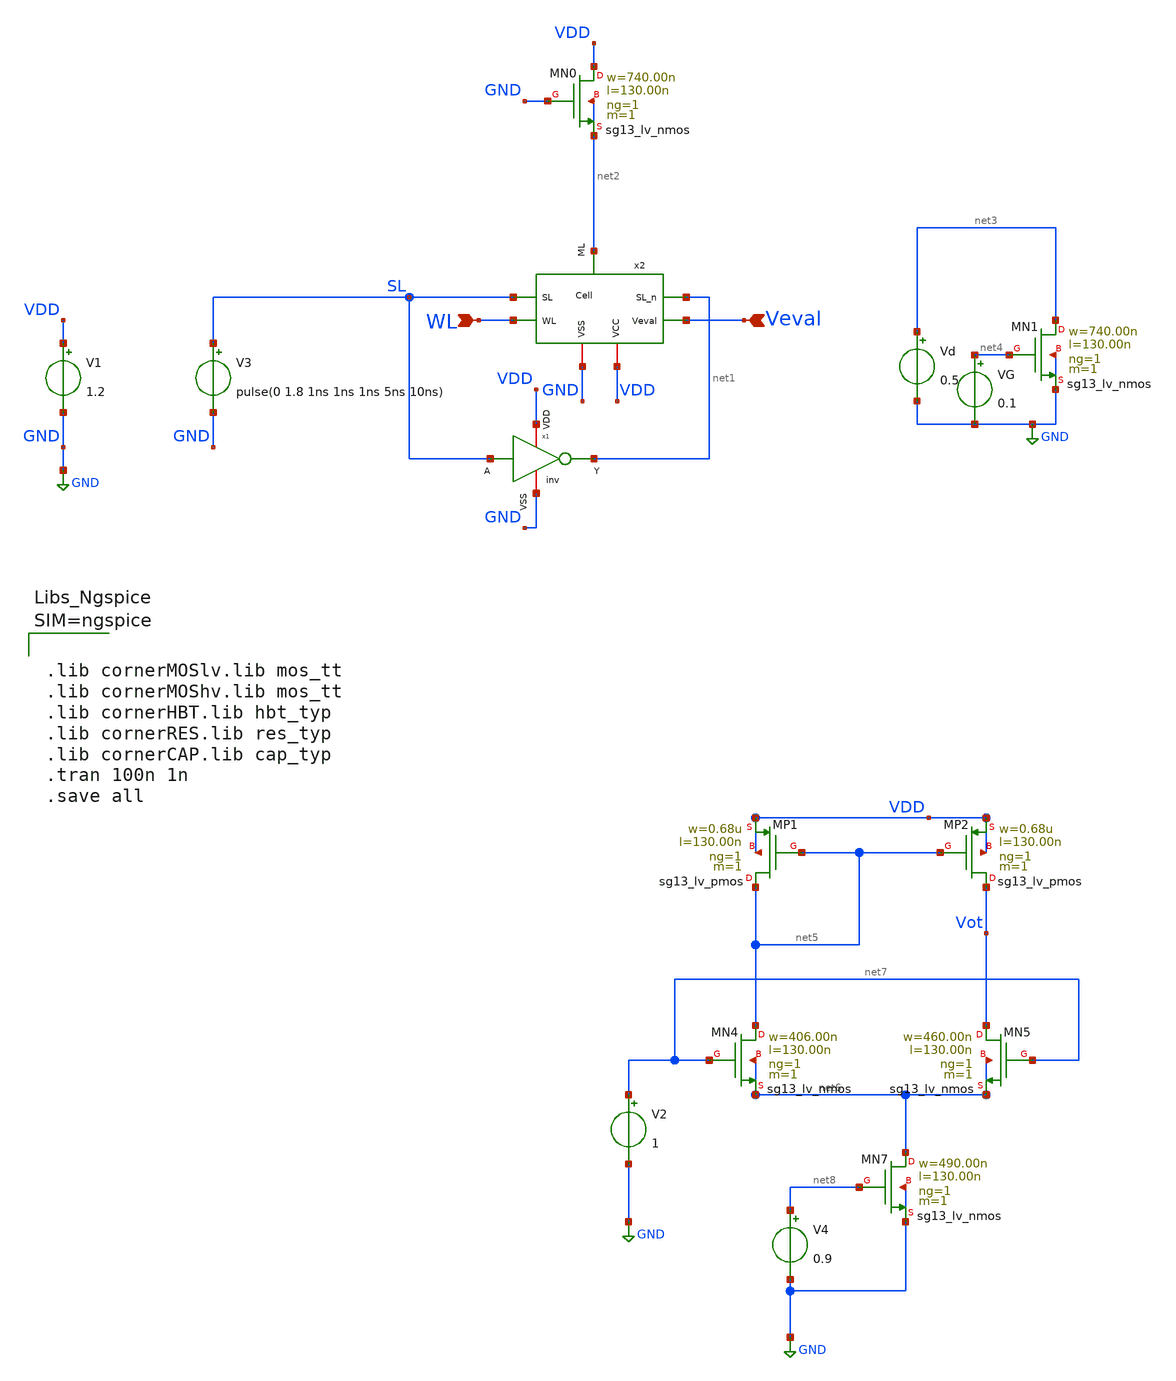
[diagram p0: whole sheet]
** sch_path: xschem/cellprobe.sch
**.subckt cellprobe WL Veval
*.ipin WL
*.ipin Veval
x2 SL WL net1 VDD net2 Veval GND Cell
V1 VDD GND 1.2
XMN0 VDD GND net2 net2 sg13_lv_nmos w=740.00n l=130.00n ng=1 m=1 mm_ok=1
V3 SL GND pulse(0 1.8 1ns 1ns 1ns 5ns 10ns)
x1 VDD net1 SL GND inv
XMN1 net3 net4 GND GND sg13_lv_nmos w=740.00n l=130.00n ng=1 m=1 mm_ok=1
Vd net3 GND 0.5
VG net4 GND 0.1
XMP1 net5 net5 VDD VDD sg13_lv_pmos w=0.68u l=130.00n ng=1 m=1 mm_ok=1
XMN4 net5 net7 net6 net6 sg13_lv_nmos w=406.00n l=130.00n ng=1 m=1 mm_ok=1
XMP2 Vot net5 VDD VDD sg13_lv_pmos w=0.68u l=130.00n ng=1 m=1 mm_ok=1
XMN5 Vot net7 net6 net6 sg13_lv_nmos w=460.00n l=130.00n ng=1 m=1 mm_ok=1
XMN7 net6 net8 GND GND sg13_lv_nmos w=490.00n l=130.00n ng=1 m=1 mm_ok=1
V4 net8 GND 0.9
V2 net7 GND 1
**** begin user architecture code



.lib cornerMOSlv.lib mos_tt
.lib cornerMOShv.lib mos_tt
.lib cornerHBT.lib hbt_typ
.lib cornerRES.lib res_typ
.lib cornerCAP.lib cap_typ
.tran 100n 1n
.save all




**** end user architecture code
**.ends
.GLOBAL GND
.end
